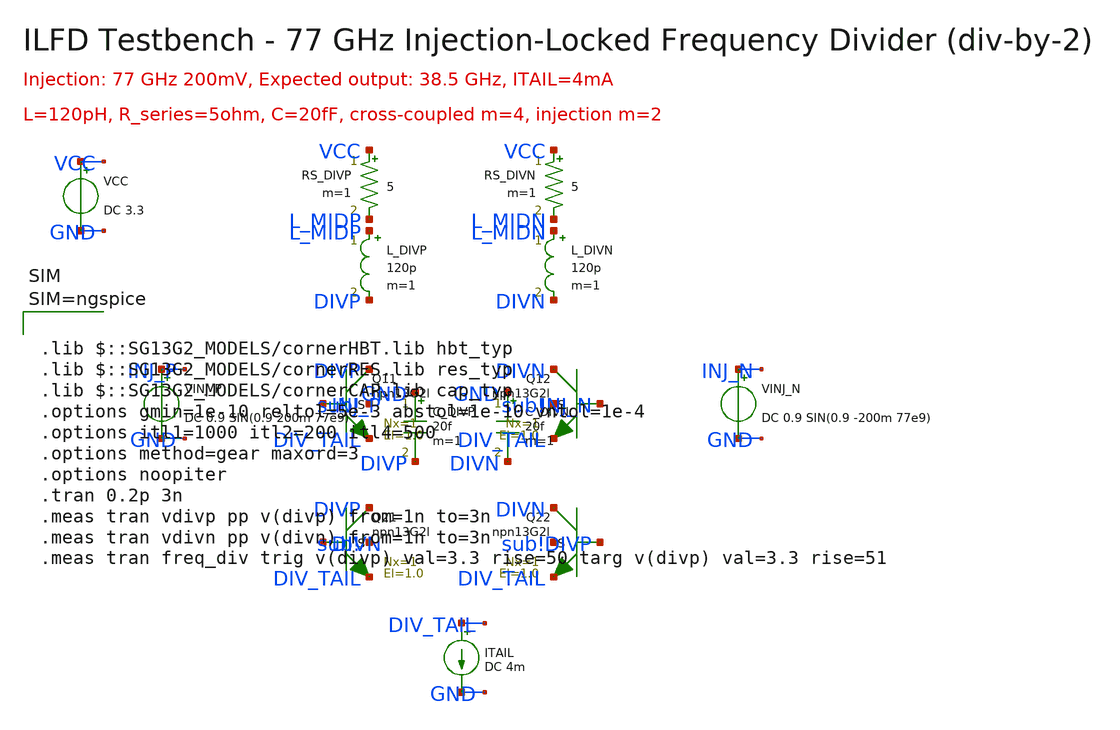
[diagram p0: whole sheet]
** sch_path: layout/testbenches/tb_ilfd.sch
**.subckt tb_ilfd
XQ21 DIVP DIVN DIV_TAIL sub! npn13G2l Nx=1 El=1.0 mm_ok=1
XQ22 DIVN DIVP DIV_TAIL sub! npn13G2l Nx=1 El=1.0 mm_ok=1
XQ11 DIVP INJ_P DIV_TAIL sub! npn13G2l Nx=1 El=1.0 mm_ok=1
XQ12 DIVN INJ_N DIV_TAIL sub! npn13G2l Nx=1 El=1.0 mm_ok=1
L_DIVP L_MIDP DIVP 120p m=1
L_DIVN L_MIDN DIVN 120p m=1
RS_DIVP VCC L_MIDP 5 m=1
RS_DIVN VCC L_MIDN 5 m=1
C_DIVP GND DIVP 20f m=1
C_DIVN GND DIVN 20f m=1
VCC VCC GND DC 3.3
ITAIL DIV_TAIL GND DC 4m
VINJ_P INJ_P GND DC 0.9 SIN(0.9 200m 77e9)
VINJ_N INJ_N GND DC 0.9 SIN(0.9 -200m 77e9)
**** begin user architecture code



.lib $::SG13G2_MODELS/cornerHBT.lib hbt_typ
.lib $::SG13G2_MODELS/cornerRES.lib res_typ
.lib $::SG13G2_MODELS/cornerCAP.lib cap_typ
.options gmin=1e-10 reltol=5e-3 abstol=1e-10 vntol=1e-4
.options itl1=1000 itl2=200 itl4=500
.options method=gear maxord=3
.options noopiter
.tran 0.2p 3n
.meas tran vdivp pp v(divp) from=1n to=3n
.meas tran vdivn pp v(divn) from=1n to=3n
.meas tran freq_div trig v(divp) val=3.3 rise=50 targ v(divp) val=3.3 rise=51



**** end user architecture code
**.ends
.end
